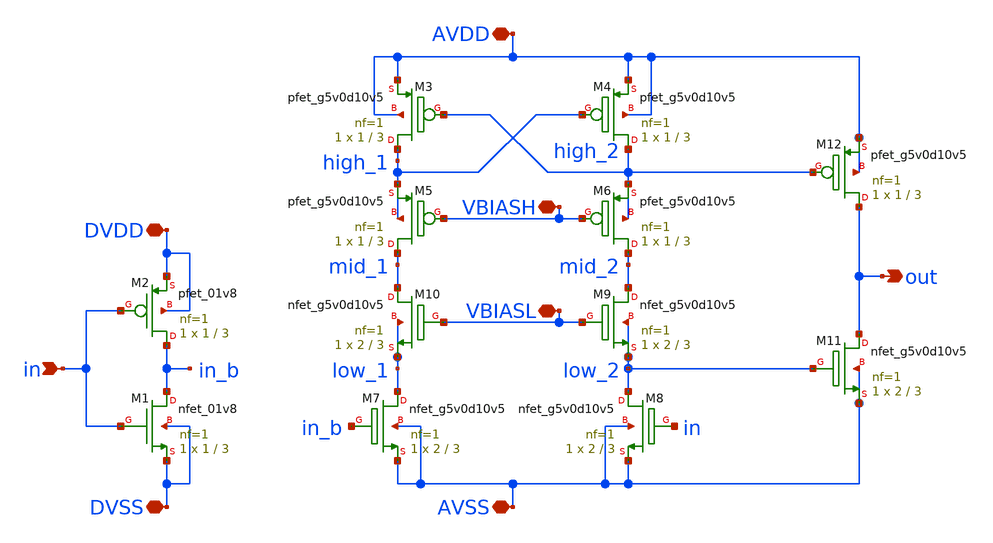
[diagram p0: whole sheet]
** sch_path: xschem/level_shifter.sch
**.subckt level_shifter AVDD out AVSS DVDD in DVSS VBIASH VBIASL
*.iopin AVDD
*.opin out
*.iopin AVSS
*.iopin DVDD
*.ipin in
*.iopin DVSS
*.iopin VBIASH
*.iopin VBIASL
XM1 in_b in DVSS DVSS sky130_fd_pr__nfet_01v8 L=3 W=1 nf=1 ad='int((nf+1)/2) * W/nf * 0.29' as='int((nf+2)/2) * W/nf * 0.29'
+ pd='2*int((nf+1)/2) * (W/nf + 0.29)' ps='2*int((nf+2)/2) * (W/nf + 0.29)' nrd='0.29 / W' nrs='0.29 / W'
+ sa=0 sb=0 sd=0 mult=1 m=1
XM2 in_b in DVDD DVDD sky130_fd_pr__pfet_01v8 L=3 W=1 nf=1 ad='int((nf+1)/2) * W/nf * 0.29' as='int((nf+2)/2) * W/nf * 0.29'
+ pd='2*int((nf+1)/2) * (W/nf + 0.29)' ps='2*int((nf+2)/2) * (W/nf + 0.29)' nrd='0.29 / W' nrs='0.29 / W'
+ sa=0 sb=0 sd=0 mult=1 m=1
XM3 high_1 high_2 AVDD AVDD sky130_fd_pr__pfet_g5v0d10v5 L=3 W=1 nf=1 ad='int((nf+1)/2) * W/nf * 0.29'
+ as='int((nf+2)/2) * W/nf * 0.29' pd='2*int((nf+1)/2) * (W/nf + 0.29)' ps='2*int((nf+2)/2) * (W/nf + 0.29)'
+ nrd='0.29 / W' nrs='0.29 / W' sa=0 sb=0 sd=0 mult=1 m=1
XM4 high_2 high_1 AVDD AVDD sky130_fd_pr__pfet_g5v0d10v5 L=3 W=1 nf=1 ad='int((nf+1)/2) * W/nf * 0.29'
+ as='int((nf+2)/2) * W/nf * 0.29' pd='2*int((nf+1)/2) * (W/nf + 0.29)' ps='2*int((nf+2)/2) * (W/nf + 0.29)'
+ nrd='0.29 / W' nrs='0.29 / W' sa=0 sb=0 sd=0 mult=1 m=1
XM8 low_2 in AVSS AVSS sky130_fd_pr__nfet_g5v0d10v5 L=3 W=2 nf=1 ad='int((nf+1)/2) * W/nf * 0.29' as='int((nf+2)/2) * W/nf * 0.29'
+ pd='2*int((nf+1)/2) * (W/nf + 0.29)' ps='2*int((nf+2)/2) * (W/nf + 0.29)' nrd='0.29 / W' nrs='0.29 / W'
+ sa=0 sb=0 sd=0 mult=1 m=1
XM7 low_1 in_b AVSS AVSS sky130_fd_pr__nfet_g5v0d10v5 L=3 W=2 nf=1 ad='int((nf+1)/2) * W/nf * 0.29' as='int((nf+2)/2) * W/nf * 0.29'
+ pd='2*int((nf+1)/2) * (W/nf + 0.29)' ps='2*int((nf+2)/2) * (W/nf + 0.29)' nrd='0.29 / W' nrs='0.29 / W'
+ sa=0 sb=0 sd=0 mult=1 m=1
XM5 mid_1 VBIASH high_1 high_1 sky130_fd_pr__pfet_g5v0d10v5 L=3 W=1 nf=1 ad='int((nf+1)/2) * W/nf * 0.29'
+ as='int((nf+2)/2) * W/nf * 0.29' pd='2*int((nf+1)/2) * (W/nf + 0.29)' ps='2*int((nf+2)/2) * (W/nf + 0.29)'
+ nrd='0.29 / W' nrs='0.29 / W' sa=0 sb=0 sd=0 mult=1 m=1
XM6 mid_2 VBIASH high_2 high_2 sky130_fd_pr__pfet_g5v0d10v5 L=3 W=1 nf=1 ad='int((nf+1)/2) * W/nf * 0.29'
+ as='int((nf+2)/2) * W/nf * 0.29' pd='2*int((nf+1)/2) * (W/nf + 0.29)' ps='2*int((nf+2)/2) * (W/nf + 0.29)'
+ nrd='0.29 / W' nrs='0.29 / W' sa=0 sb=0 sd=0 mult=1 m=1
XM9 mid_2 VBIASL low_2 low_2 sky130_fd_pr__nfet_g5v0d10v5 L=3 W=2 nf=1 ad='int((nf+1)/2) * W/nf * 0.29'
+ as='int((nf+2)/2) * W/nf * 0.29' pd='2*int((nf+1)/2) * (W/nf + 0.29)' ps='2*int((nf+2)/2) * (W/nf + 0.29)'
+ nrd='0.29 / W' nrs='0.29 / W' sa=0 sb=0 sd=0 mult=1 m=1
XM10 mid_1 VBIASL low_1 low_1 sky130_fd_pr__nfet_g5v0d10v5 L=3 W=2 nf=1 ad='int((nf+1)/2) * W/nf * 0.29'
+ as='int((nf+2)/2) * W/nf * 0.29' pd='2*int((nf+1)/2) * (W/nf + 0.29)' ps='2*int((nf+2)/2) * (W/nf + 0.29)'
+ nrd='0.29 / W' nrs='0.29 / W' sa=0 sb=0 sd=0 mult=1 m=1
XM11 out low_2 AVSS AVSS sky130_fd_pr__nfet_g5v0d10v5 L=3 W=2 nf=1 ad='int((nf+1)/2) * W/nf * 0.29' as='int((nf+2)/2) * W/nf * 0.29'
+ pd='2*int((nf+1)/2) * (W/nf + 0.29)' ps='2*int((nf+2)/2) * (W/nf + 0.29)' nrd='0.29 / W' nrs='0.29 / W'
+ sa=0 sb=0 sd=0 mult=1 m=1
XM12 out high_2 AVDD AVDD sky130_fd_pr__pfet_g5v0d10v5 L=3 W=1 nf=1 ad='int((nf+1)/2) * W/nf * 0.29'
+ as='int((nf+2)/2) * W/nf * 0.29' pd='2*int((nf+1)/2) * (W/nf + 0.29)' ps='2*int((nf+2)/2) * (W/nf + 0.29)'
+ nrd='0.29 / W' nrs='0.29 / W' sa=0 sb=0 sd=0 mult=1 m=1
**.ends
.end
